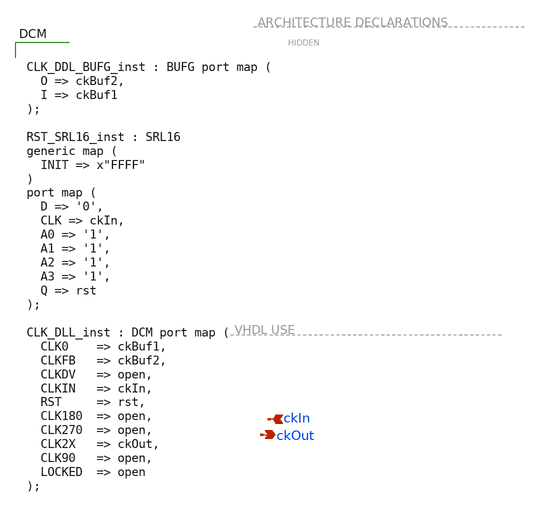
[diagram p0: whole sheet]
** sch_path: xschem/CLK_DLL.sch
**.subckt CLK_DLL ckIn ckOut
*.ipin ckIn
*.opin ckOut
**** begin user architecture code


CLK_DDL_BUFG_inst : BUFG port map (
  O => ckBuf2,
  I => ckBuf1
);

RST_SRL16_inst : SRL16
generic map (
  INIT => x"FFFF"
)
port map (
  D => '0',
  CLK => ckIn,
  A0 => '1',
  A1 => '1',
  A2 => '1',
  A3 => '1',
  Q => rst
);

CLK_DLL_inst : DCM port map (
  CLK0    => ckBuf1,
  CLKFB   => ckBuf2,
  CLKDV   => open,
  CLKIN   => ckIn,
  RST     => rst,
  CLK180  => open,
  CLK270  => open,
  CLK2X   => ckOut,
  CLK90   => open,
  LOCKED  => open
);


**** end user architecture code
**.ends
.end
